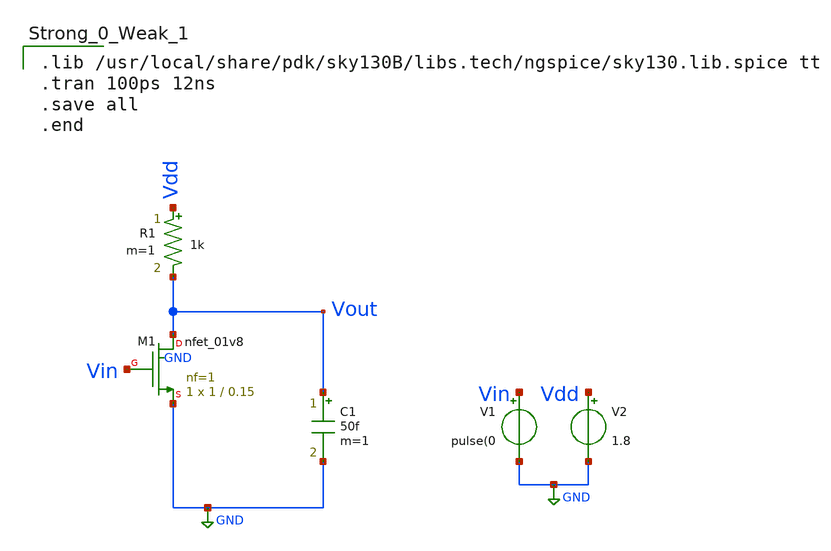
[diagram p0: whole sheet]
** sch_path: Xschem/nmos_test.sch
**.subckt nmos_test
XM1 Vout Vin GND GND sky130_fd_pr__nfet_01v8 L=0.15 W=1 nf=1 ad='int((nf+1)/2) * W/nf * 0.29' as='int((nf+2)/2) * W/nf * 0.29'
+ pd='2*int((nf+1)/2) * (W/nf + 0.29)' ps='2*int((nf+2)/2) * (W/nf + 0.29)' nrd='0.29 / W' nrs='0.29 / W'
+ sa=0 sb=0 sd=0 mult=1 m=1
R1 Vdd Vout 1k m=1
C1 Vout GND 50f m=1
V1 Vin GND pulse(0
V2 Vdd GND 1.8
**** begin user architecture code

.lib /usr/local/share/pdk/sky130B/libs.tech/ngspice/sky130.lib.spice tt
.tran 100ps 12ns
.save all
.end

**** end user architecture code
**.ends
.GLOBAL GND
.end
